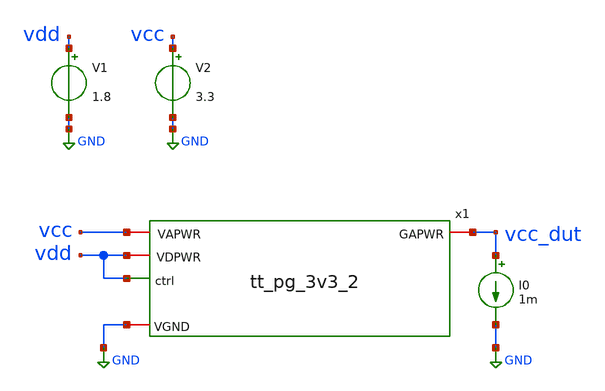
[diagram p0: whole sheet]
** sch_path: pg/sky130/tt_pg_3v3_2/xschem/tb_rdson.sch
**.subckt tb_rdson
x1 GND vdd vcc vdd vcc_dut tt_pg_3v3_2
V2 vcc GND 3.3
I0 vcc_dut GND 1m
V1 vdd GND 1.8
**** begin user architecture code

** opencircuitdesign pdks install
.lib $::SKYWATER_MODELS/sky130.lib.spice tt
.include $::SKYWATER_STDCELLS/sky130_fd_sc_hd.spice





.param mc_mm_switch=0
.control
save all
dc V2 2 5.5 0.05
plot ((v(vcc) - v(vcc_dut)) / 1m)
write tb_rdson.raw
*quit 0
.endc
.end


**** end user architecture code
**.ends
.GLOBAL GND
.end
